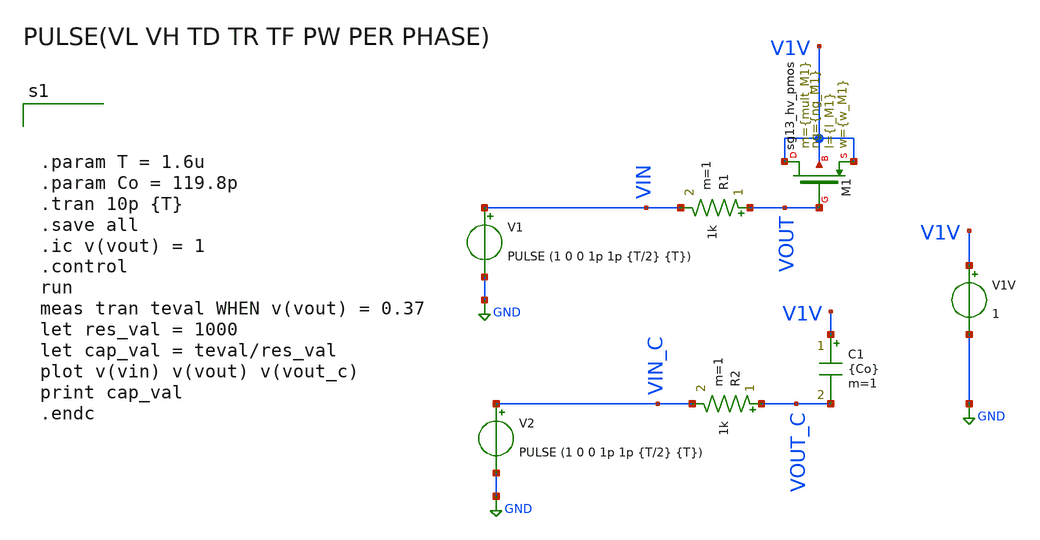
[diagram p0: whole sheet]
** sch_path: xschem/DCDCBuck/TB_powerPMOS_cgate_ext.sch
**.subckt TB_powerPMOS_cgate_ext
R1 VOUT VIN 1k m=1
V1 VIN GND PULSE (1 0 0 1p 1p {T/2} {T})
V1V V1V GND 1
R2 VOUT_C VIN_C 1k m=1
V2 VIN_C GND PULSE (1 0 0 1p 1p {T/2} {T})
C1 V1V VOUT_C {Co} m=1
XM1 V1V VOUT V1V V1V sg13_hv_pmos w={w_M1} l={l_M1} ng={ng_M1} m={mult_M1} mm_ok=1
**** begin user architecture code



.param T = 1.6u
.param Co = 119.8p
.tran 10p {T}
.save all
.ic v(vout) = 1
.control
run
meas tran teval WHEN v(vout) = 0.37
let res_val = 1000
let cap_val = teval/res_val
plot v(vin) v(vout) v(vout_c)
print cap_val
.endc




.lib cornerMOShv.lib mos_tt
.lib cornerMOSlv.lib mos_tt
*.lib cornerMOShv.lib mos_ff
*.lib cornerMOSlv.lib mos_ff
*.lib cornerMOShv.lib mos_ss
*.lib cornerMOSlv.lib mos_ss
*.lib cornerMOShv.lib mos_sf
*.lib cornerMOSlv.lib mos_sf
*.lib cornerMOShv.lib mos_fs
*.lib cornerMOSlv.lib mos_fs

.include /opt/pdks/ihp-sg13g2/libs.ref/sg13g2_stdcell/spice/sg13g2_stdcell.spice
.lib $::SG13G2_MODELS/cornerRES.lib res_typ
.lib $::SG13G2_MODELS/cornerCAP.lib cap_typ
*.lib $::SG13G2_MODELS/diodes.lib



.param mult = 95238
.param temp=27
.param mult_M1 = 3*mult
.param w_M1 =0.3u
.param l_M1 = 0.45u
.param ng_M1 = 1

.param mult_M2 = 1*mult
.param w_M2 =0.3u
.param l_M2 =0.45u
.param ng_M2 =1





**** end user architecture code
**.ends
.GLOBAL GND
.end
